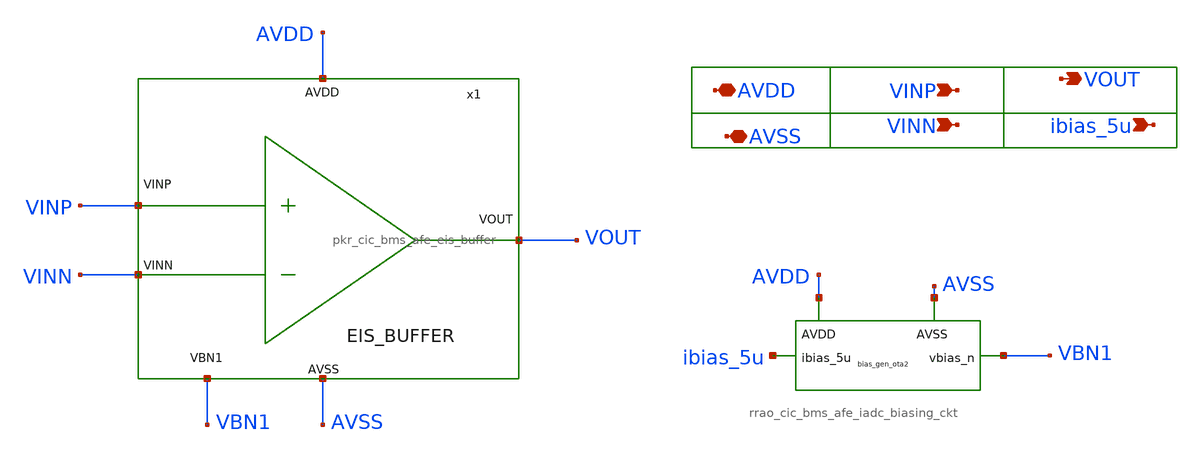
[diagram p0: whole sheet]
** sch_path: design/schematics/EIS/pkr_eis_DAC_buffer_w_bias.sch
**.subckt pkr_eis_DAC_buffer_w_bias AVDD AVSS VINP VINN VOUT ibias_5u
*.iopin AVDD
*.iopin AVSS
*.ipin VINP
*.ipin VINN
*.opin VOUT
*.ipin ibias_5u
x1 AVDD VINN VOUT VBN1 AVSS VINP pkr_cic_bms_afe_eis_buffer
x3 AVDD AVSS ibias_5u VBN1 rrao_cic_bms_afe_iadc_biasing_ckt
**.ends
.end
